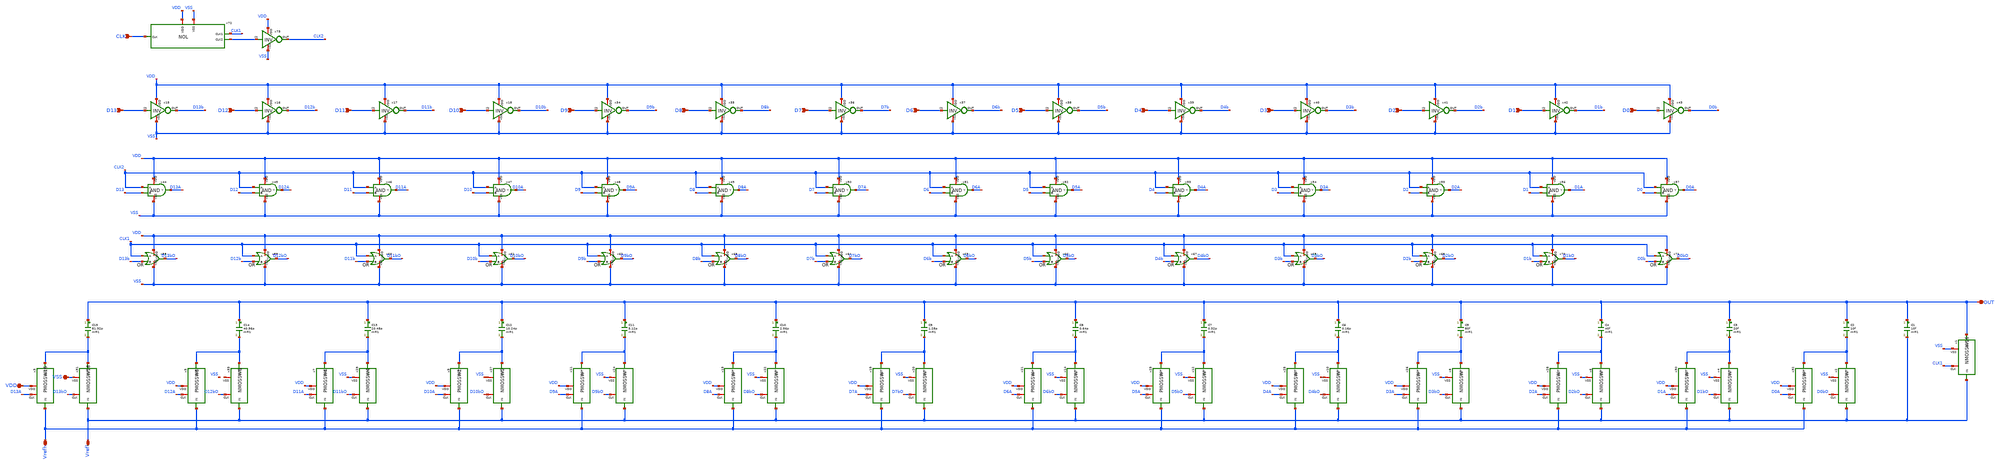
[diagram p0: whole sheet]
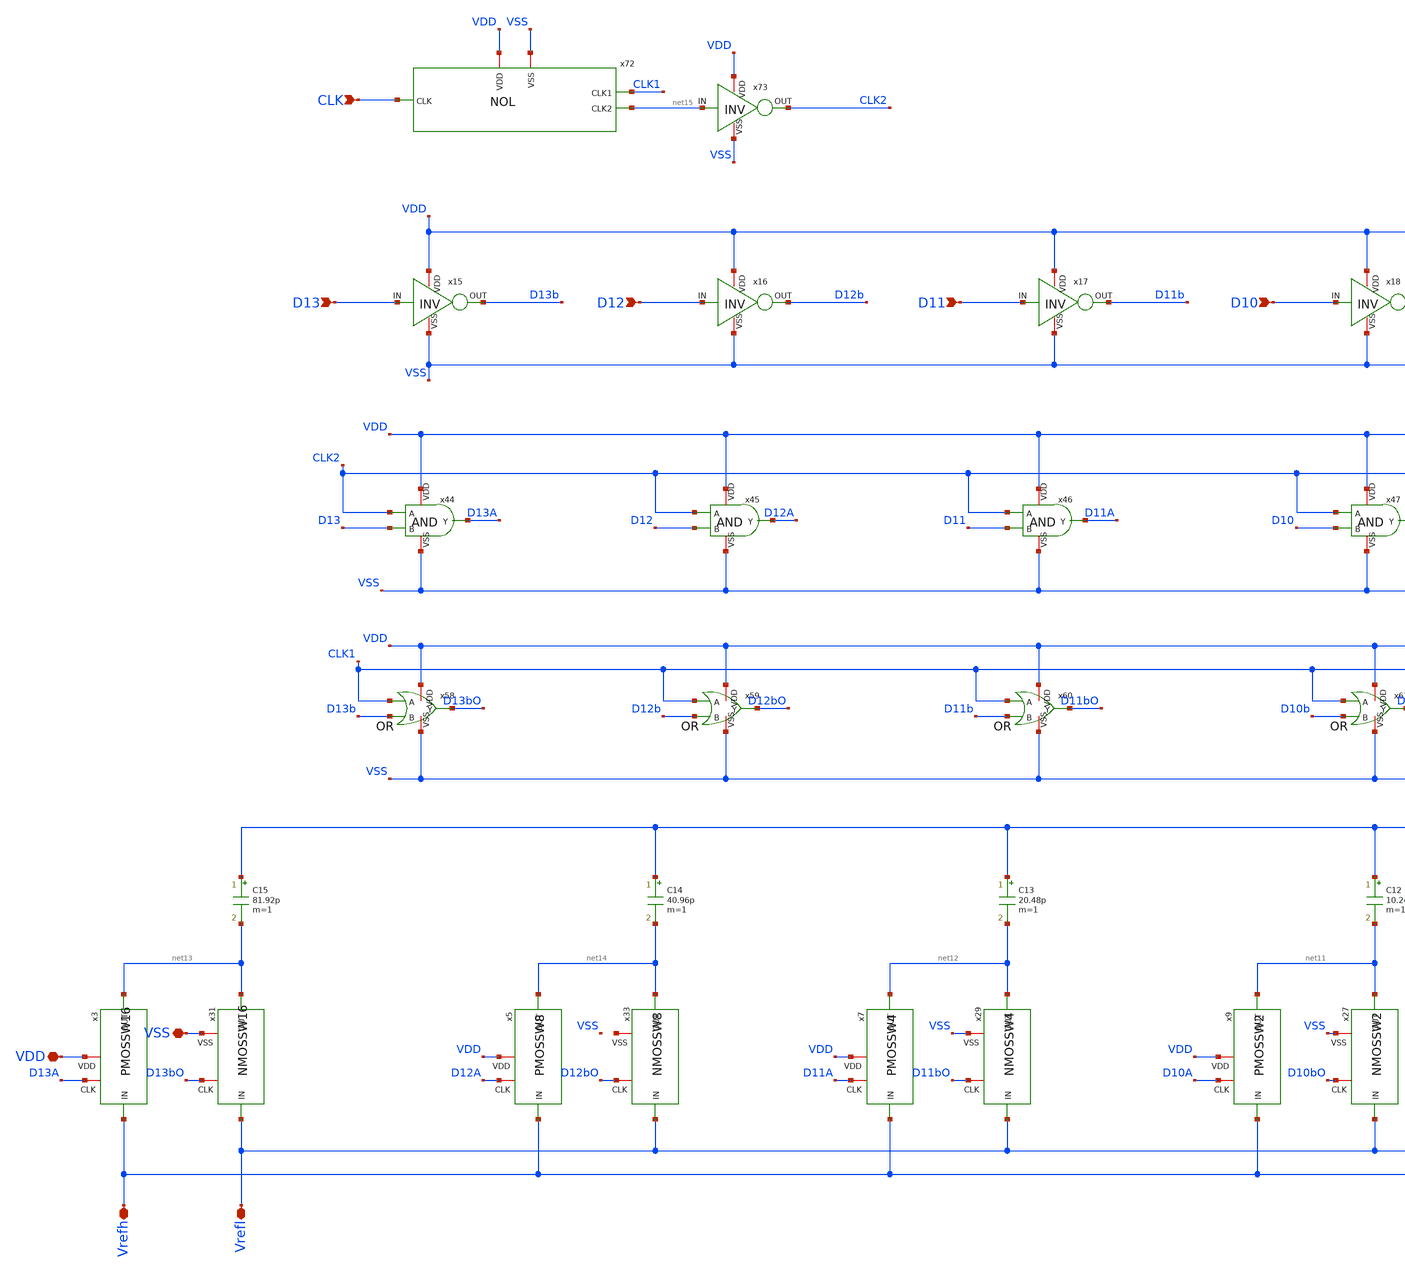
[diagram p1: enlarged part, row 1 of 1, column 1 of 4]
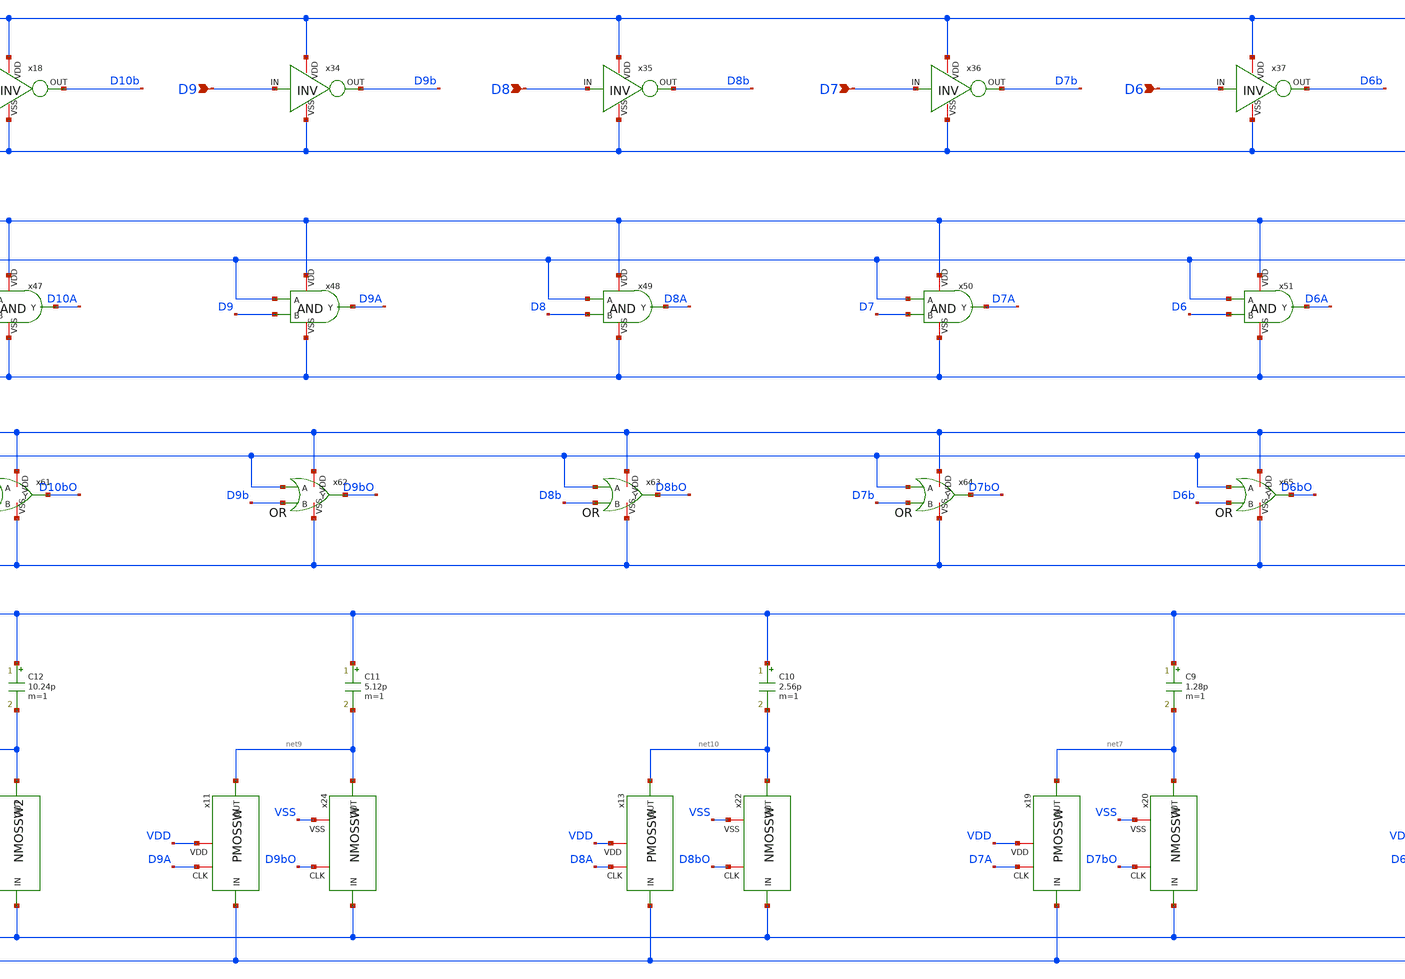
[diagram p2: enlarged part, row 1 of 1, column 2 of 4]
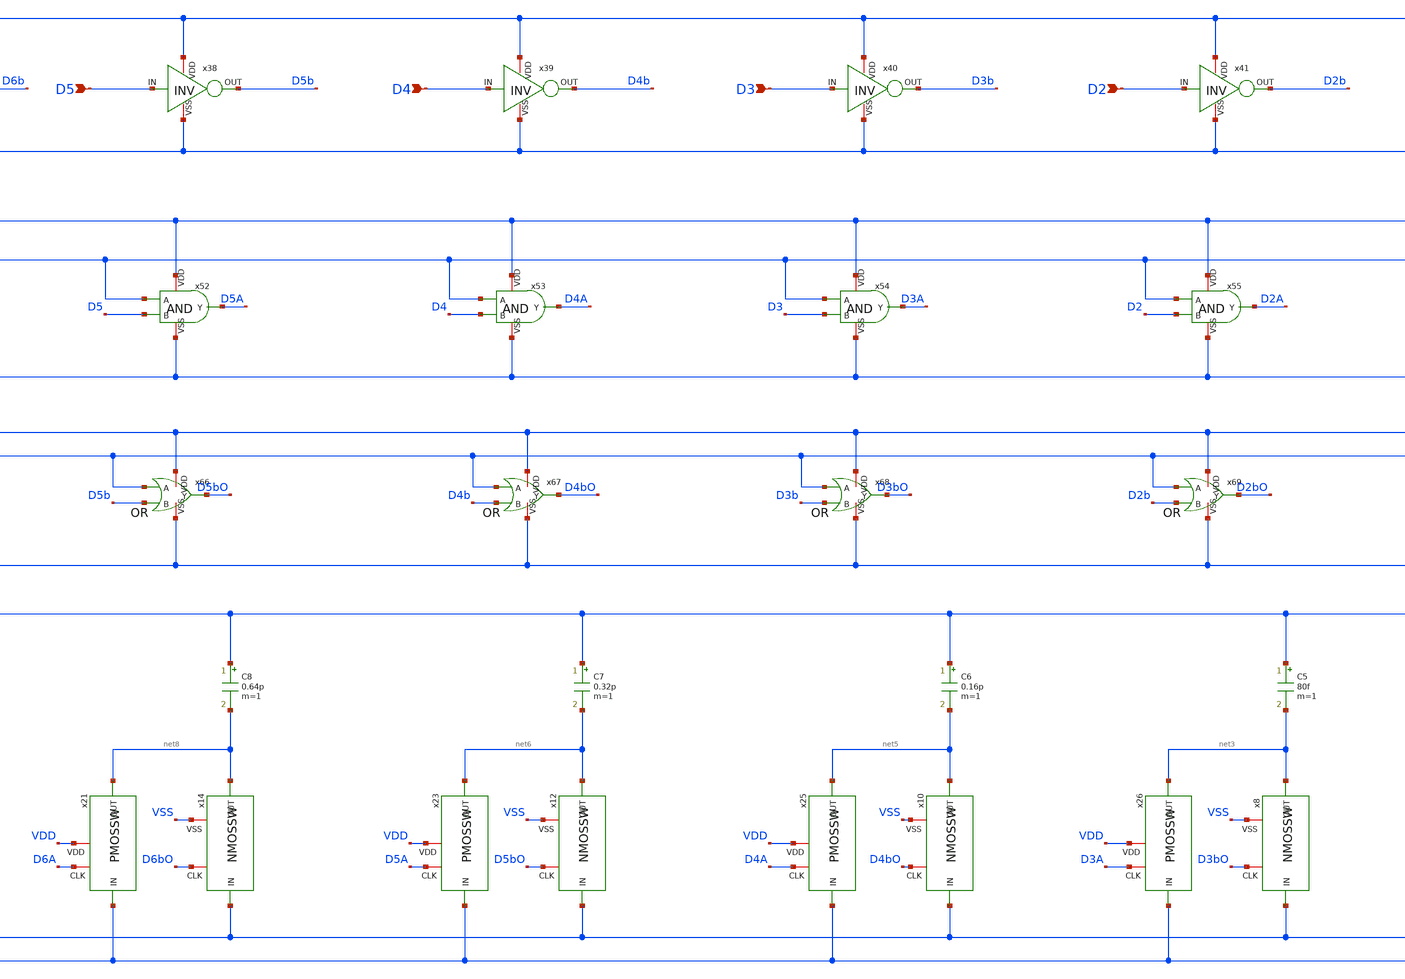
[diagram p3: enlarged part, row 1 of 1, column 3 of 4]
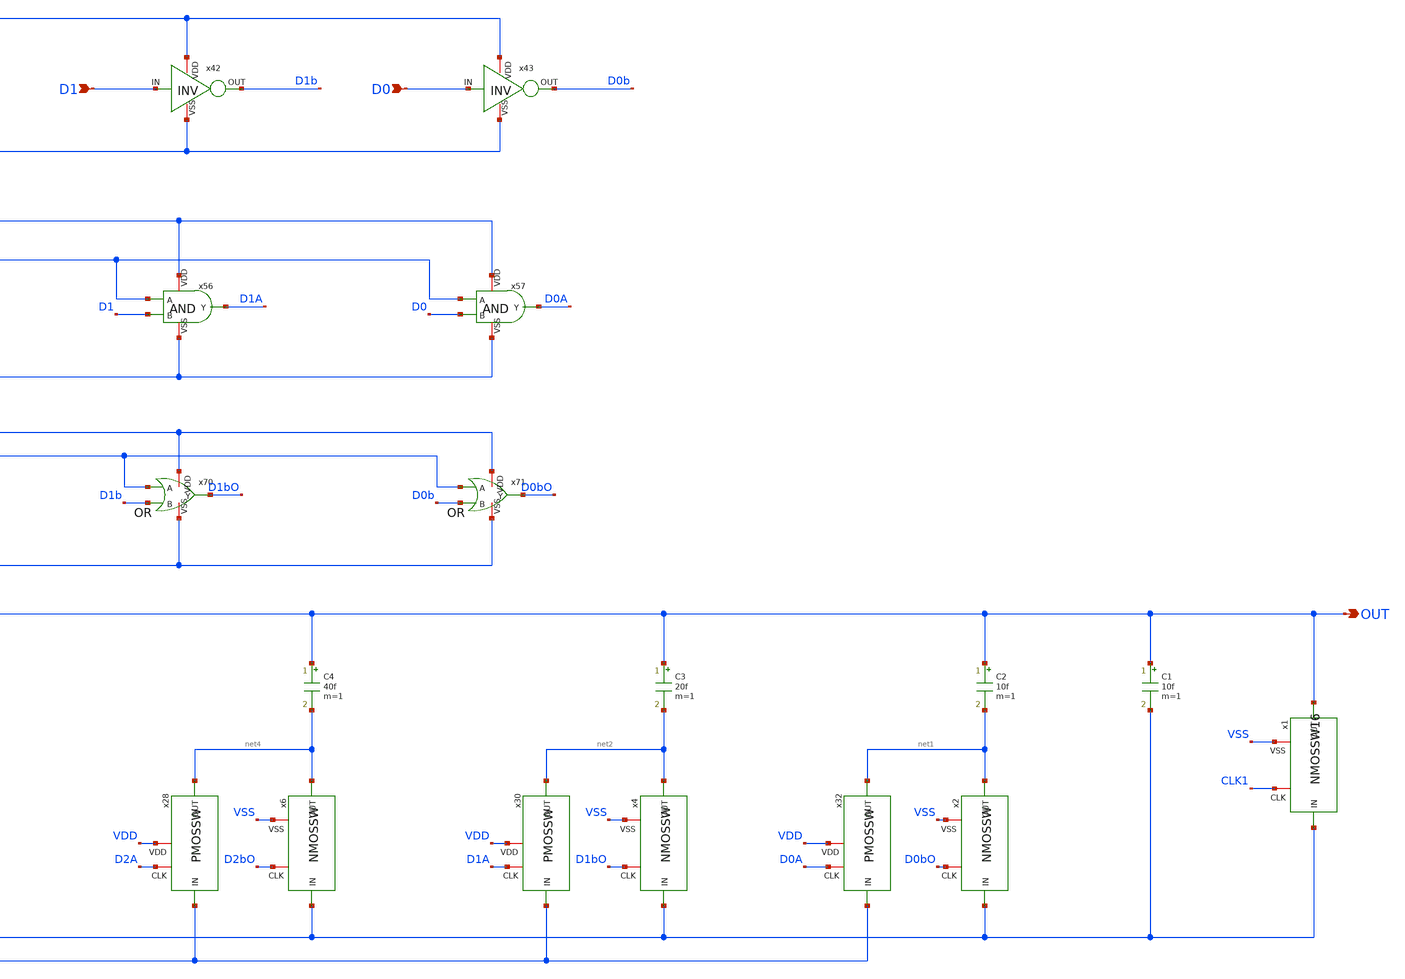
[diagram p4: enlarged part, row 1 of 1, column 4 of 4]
** sch_path: CDAC_PNSW.sch
**.subckt CDAC_PNSW OUT Vrefh Vrefl D13 D12 D11 D10 VSS VDD D9 D8 D7 D6 D5 D4 D3 D2 D1 D0 CLK
*.opin OUT
*.iopin Vrefh
*.iopin Vrefl
*.ipin D13
*.ipin D12
*.ipin D11
*.ipin D10
*.iopin VSS
*.iopin VDD
*.ipin D9
*.ipin D8
*.ipin D7
*.ipin D6
*.ipin D5
*.ipin D4
*.ipin D3
*.ipin D2
*.ipin D1
*.ipin D0
*.ipin CLK
C1 OUT Vrefl 10f m=1
C2 OUT net1 10f m=1
C3 OUT net2 20f m=1
C4 OUT net4 40f m=1
C5 OUT net3 80f m=1
x15 VDD D13b D13 VSS INV
x16 VDD D12b D12 VSS INV
x17 VDD D11b D11 VSS INV
x18 VDD D10b D10 VSS INV
C6 OUT net5 0.16p m=1
C7 OUT net6 0.32p m=1
C8 OUT net8 0.64p m=1
C9 OUT net7 1.28p m=1
C10 OUT net10 2.56p m=1
C11 OUT net9 5.12p m=1
C12 OUT net11 10.24p m=1
C13 OUT net12 20.48p m=1
C14 OUT net14 40.96p m=1
C15 OUT net13 81.92p m=1
x34 VDD D9b D9 VSS INV
x35 VDD D8b D8 VSS INV
x36 VDD D7b D7 VSS INV
x37 VDD D6b D6 VSS INV
x38 VDD D5b D5 VSS INV
x39 VDD D4b D4 VSS INV
x40 VDD D3b D3 VSS INV
x41 VDD D2b D2 VSS INV
x42 VDD D1b D1 VSS INV
x43 VDD D0b D0 VSS INV
x44 VDD D13A CLK2 D13 VSS AND
x45 VDD D12A CLK2 D12 VSS AND
x46 VDD D11A CLK2 D11 VSS AND
x47 VDD D10A CLK2 D10 VSS AND
x48 VDD D9A CLK2 D9 VSS AND
x49 VDD D8A CLK2 D8 VSS AND
x50 VDD D7A CLK2 D7 VSS AND
x51 VDD D6A CLK2 D6 VSS AND
x52 VDD D5A CLK2 D5 VSS AND
x53 VDD D4A CLK2 D4 VSS AND
x54 VDD D3A CLK2 D3 VSS AND
x55 VDD D2A CLK2 D2 VSS AND
x56 VDD D1A CLK2 D1 VSS AND
x57 VDD D0A CLK2 D0 VSS AND
x58 VDD CLK1 D13bO D13b VSS OR
x59 VDD CLK1 D12bO D12b VSS OR
x60 VDD CLK1 D11bO D11b VSS OR
x61 VDD CLK1 D10bO D10b VSS OR
x62 VDD CLK1 D9bO D9b VSS OR
x63 VDD CLK1 D8bO D8b VSS OR
x64 VDD CLK1 D7bO D7b VSS OR
x65 VDD CLK1 D6bO D6b VSS OR
x66 VDD CLK1 D5bO D5b VSS OR
x67 VDD CLK1 D4bO D4b VSS OR
x68 VDD CLK1 D3bO D3b VSS OR
x69 VDD CLK1 D2bO D2b VSS OR
x70 VDD CLK1 D1bO D1b VSS OR
x71 VDD CLK1 D0bO D0b VSS OR
x72 VDD CLK CLK1 VSS net15 NOL
x31 D13bO VSS net13 Vrefl NMOSSW16
x33 D12bO net16 net14 Vrefl NMOSSW8
x29 D11bO VSS net12 Vrefl NMOSSW4
x27 D10bO VSS net11 Vrefl NMOSSW2
x1 CLK1 VSS OUT Vrefl NMOSSW16
x2 D0bO VSS net1 Vrefl NMOSSW
x4 D1bO VSS net2 Vrefl NMOSSW
x6 D2bO VSS net4 Vrefl NMOSSW
x8 D3bO VSS net3 Vrefl NMOSSW
x10 D4bO VSS net5 Vrefl NMOSSW
x12 D5bO VSS net6 Vrefl NMOSSW
x14 D6bO VSS net8 Vrefl NMOSSW
x20 D7bO VSS net7 Vrefl NMOSSW
x22 D8bO VSS net10 Vrefl NMOSSW
x24 D9bO VSS net9 Vrefl NMOSSW
x3 D13A net13 Vrefh VDD PMOSSW16
x5 D12A net14 Vrefh VDD PMOSSW8
x7 D11A net12 Vrefh VDD PMOSSW4
x9 D10A net11 Vrefh VDD PMOSSW2
x11 D9A net9 Vrefh VDD PMOSSW
x13 D8A net10 Vrefh VDD PMOSSW
x19 D7A net7 Vrefh VDD PMOSSW
x21 D6A net8 Vrefh VDD PMOSSW
x23 D5A net6 Vrefh VDD PMOSSW
x25 D4A net5 Vrefh VDD PMOSSW
x26 D3A net3 Vrefh VDD PMOSSW
x28 D2A net4 Vrefh VDD PMOSSW
x30 D1A net2 Vrefh VDD PMOSSW
x32 D0A net1 Vrefh VDD PMOSSW
x73 VDD CLK2 net15 VSS INV
**.ends

* expanding   symbol:  INV.sym # of pins=4
** sym_path: INV.sym
** sch_path: INV.sch
.subckt INV VDD OUT IN VSS
*.opin OUT
*.ipin IN
*.iopin VDD
*.iopin VSS
M2 OUT IN VDD VDD pch w=10u l=0.35u as=0 ps=0 ad=0 pd=0 m=1
M1 OUT IN VSS VSS nch w=5u l=0.35u as=0 ps=0 ad=0 pd=0 m=1
.ends


* expanding   symbol:  AND.sym # of pins=5
** sym_path: AND.sym
** sch_path: AND.sch
.subckt AND VDD Y A B VSS
*.iopin VDD
*.ipin A
*.ipin B
*.iopin VSS
*.opin Y
M1 net1 A net2 VSS nch w=3.5u l=0.35u as=0 ps=0 ad=0 pd=0 m=1
M2 net1 B VDD VDD pch w=3.5u l=0.35u as=0 ps=0 ad=0 pd=0 m=1
M3 net1 A VDD VDD pch w=3.5u l=0.35u as=0 ps=0 ad=0 pd=0 m=1
M4 net2 B VSS VSS nch w=3.5u l=0.35u as=0 ps=0 ad=0 pd=0 m=1
M5 Y net1 VDD VDD pch w=3.5u l=0.35u as=0 ps=0 ad=0 pd=0 m=1
M6 Y net1 VSS VSS nch w=3.5u l=0.35u as=0 ps=0 ad=0 pd=0 m=1
.ends


* expanding   symbol:  OR.sym # of pins=5
** sym_path: OR.sym
** sch_path: OR.sch
.subckt OR VDD A Y B VSS
*.iopin VDD
*.ipin A
*.ipin B
*.iopin VSS
*.opin Y
M1 net1 A VSS VSS nch w=3.5u l=0.35u as=0 ps=0 ad=0 pd=0 m=1
M2 net2 A VDD VDD pch w=3.5u l=0.35u as=0 ps=0 ad=0 pd=0 m=1
M3 net1 B net2 VDD pch w=3.5u l=0.35u as=0 ps=0 ad=0 pd=0 m=1
M4 net1 B VSS VSS nch w=3.5u l=0.35u as=0 ps=0 ad=0 pd=0 m=1
M5 Y net1 VDD VDD pch w=3.5u l=0.35u as=0 ps=0 ad=0 pd=0 m=1
M6 Y net1 VSS VSS nch w=3.5u l=0.35u as=0 ps=0 ad=0 pd=0 m=1
.ends


* expanding   symbol:  NOL.sym # of pins=5
** sym_path: NOL.sym
** sch_path: NOL.sch
.subckt NOL VDD CLK CLK1 VSS CLK2
*.ipin CLK
*.opin CLK1
*.opin CLK2
*.iopin VDD
*.iopin VSS
x3 VDD net1 CLK VSS INV
x1 VDD CLK net9 CLK2 VSS NOR
x2 VDD CLK1 net2 net1 VSS NOR
x4 VDD net3 net2 VSS INV
x5 VDD net4 net3 VSS INV
x6 VDD net5 net4 VSS INV
x7 VDD net17 net5 VSS INV
x8 VDD net6 net9 VSS INV
x9 VDD net7 net6 VSS INV
x10 VDD net8 net7 VSS INV
x11 VDD net13 net8 VSS INV
x12 VDD net10 net13 VSS INV
x13 VDD net11 net10 VSS INV
x14 VDD net12 net11 VSS INV
x15 VDD net32 net12 VSS INV
x16 VDD net14 net17 VSS INV
x17 VDD net15 net14 VSS INV
x18 VDD net16 net15 VSS INV
x19 VDD net33 net16 VSS INV
x20 VDD net18 net33 VSS INV
x21 VDD net19 net18 VSS INV
x22 VDD net20 net19 VSS INV
x23 VDD net24 net20 VSS INV
x24 VDD net21 net24 VSS INV
x25 VDD net22 net21 VSS INV
x26 VDD net23 net22 VSS INV
x27 VDD CLK2 net23 VSS INV
x28 VDD net25 net32 VSS INV
x29 VDD net26 net25 VSS INV
x30 VDD net27 net26 VSS INV
x31 VDD net31 net27 VSS INV
x32 VDD net28 net31 VSS INV
x33 VDD net29 net28 VSS INV
x34 VDD net30 net29 VSS INV
x35 VDD CLK1 net30 VSS INV
.ends


* expanding   symbol:  NMOSSW16.sym # of pins=4
** sym_path: NMOSSW16.sym
** sch_path: NMOSSW16.sch
.subckt NMOSSW16 CLK VSS OUT IN
*.ipin IN
*.opin OUT
*.iopin VSS
*.iopin CLK
x1 CLK VSS OUT IN NMOSSW8
x2 CLK VSS OUT IN NMOSSW8
.ends


* expanding   symbol:  NMOSSW8.sym # of pins=4
** sym_path: NMOSSW8.sym
** sch_path: NMOSSW8.sch
.subckt NMOSSW8 CLK VSS OUT IN
*.ipin IN
*.opin OUT
*.iopin VSS
*.iopin CLK
x1 CLK VSS OUT IN NMOSSW4
x2 CLK VSS OUT IN NMOSSW4
.ends


* expanding   symbol:  NMOSSW4.sym # of pins=4
** sym_path: NMOSSW4.sym
** sch_path: NMOSSW4.sch
.subckt NMOSSW4 CLK VSS OUT IN
*.ipin IN
*.opin OUT
*.iopin VSS
*.iopin CLK
x1 CLK VSS OUT IN NMOSSW2
x2 CLK VSS OUT IN NMOSSW2
.ends


* expanding   symbol:  NMOSSW2.sym # of pins=4
** sym_path: NMOSSW2.sym
** sch_path: NMOSSW2.sch
.subckt NMOSSW2 CLK VSS OUT IN
*.ipin IN
*.opin OUT
*.iopin VSS
*.iopin CLK
x1 CLK VSS OUT IN NMOSSW
x2 CLK VSS OUT IN NMOSSW
.ends


* expanding   symbol:  NMOSSW.sym # of pins=4
** sym_path: NMOSSW.sym
** sch_path: NMOSSW.sch
.subckt NMOSSW CLK VSS OUT IN
*.ipin IN
*.iopin VSS
*.opin OUT
*.iopin CLK
M1 OUT CLK IN VSS nch w=10u l=0.35u as=0 ps=0 ad=0 pd=0 m=1
.ends


* expanding   symbol:  PMOSSW16.sym # of pins=4
** sym_path: PMOSSW16.sym
** sch_path: PMOSSW16.sch
.subckt PMOSSW16 CLK OUT IN VDD
*.ipin IN
*.opin OUT
*.iopin CLK
*.iopin VDD
x1 CLK OUT IN VDD PMOSSW8
x2 CLK OUT IN VDD PMOSSW8
.ends


* expanding   symbol:  PMOSSW8.sym # of pins=4
** sym_path: PMOSSW8.sym
** sch_path: PMOSSW8.sch
.subckt PMOSSW8 CLK OUT IN VDD
*.ipin IN
*.opin OUT
*.iopin CLK
*.iopin VDD
x1 CLK OUT IN VDD PMOSSW4
x2 CLK OUT IN VDD PMOSSW4
.ends


* expanding   symbol:  PMOSSW4.sym # of pins=4
** sym_path: PMOSSW4.sym
** sch_path: PMOSSW4.sch
.subckt PMOSSW4 CLK OUT IN VDD
*.ipin IN
*.opin OUT
*.iopin CLK
*.iopin VDD
x1 CLK OUT IN VDD PMOSSW2
x2 CLK OUT IN VDD PMOSSW2
.ends


* expanding   symbol:  PMOSSW2.sym # of pins=4
** sym_path: PMOSSW2.sym
** sch_path: PMOSSW2.sch
.subckt PMOSSW2 CLK OUT IN VDD
*.ipin IN
*.opin OUT
*.iopin CLK
*.iopin VDD
x1 CLK OUT IN VDD PMOSSW
x2 CLK OUT IN VDD PMOSSW
.ends


* expanding   symbol:  PMOSSW.sym # of pins=4
** sym_path: PMOSSW.sym
** sch_path: PMOSSW.sch
.subckt PMOSSW CLK OUT IN VDD
*.ipin IN
*.opin OUT
*.iopin VDD
*.iopin CLK
M5 OUT CLK IN VDD pch w=10u l=0.35u as=0 ps=0 ad=0 pd=0 m=1
.ends


* expanding   symbol:  NOR.sym # of pins=5
** sym_path: NOR.sym
** sch_path: NOR.sch
.subckt NOR VDD A Y B VSS
*.iopin VDD
*.ipin A
*.ipin B
*.iopin VSS
*.opin Y
M1 Y A VSS VSS nch w=3.5u l=0.35u as=0 ps=0 ad=0 pd=0 m=1
M2 net1 A VDD VDD pch w=3.5u l=0.35u as=0 ps=0 ad=0 pd=0 m=1
M3 Y B net1 VDD pch w=3.5u l=0.35u as=0 ps=0 ad=0 pd=0 m=1
M4 Y B VSS VSS nch w=3.5u l=0.35u as=0 ps=0 ad=0 pd=0 m=1
.ends

.end
